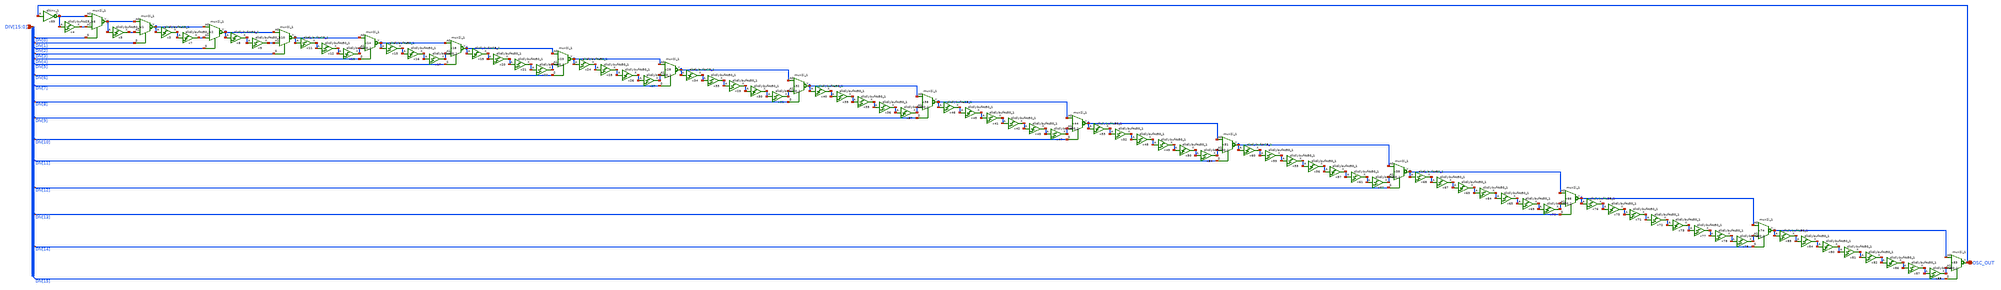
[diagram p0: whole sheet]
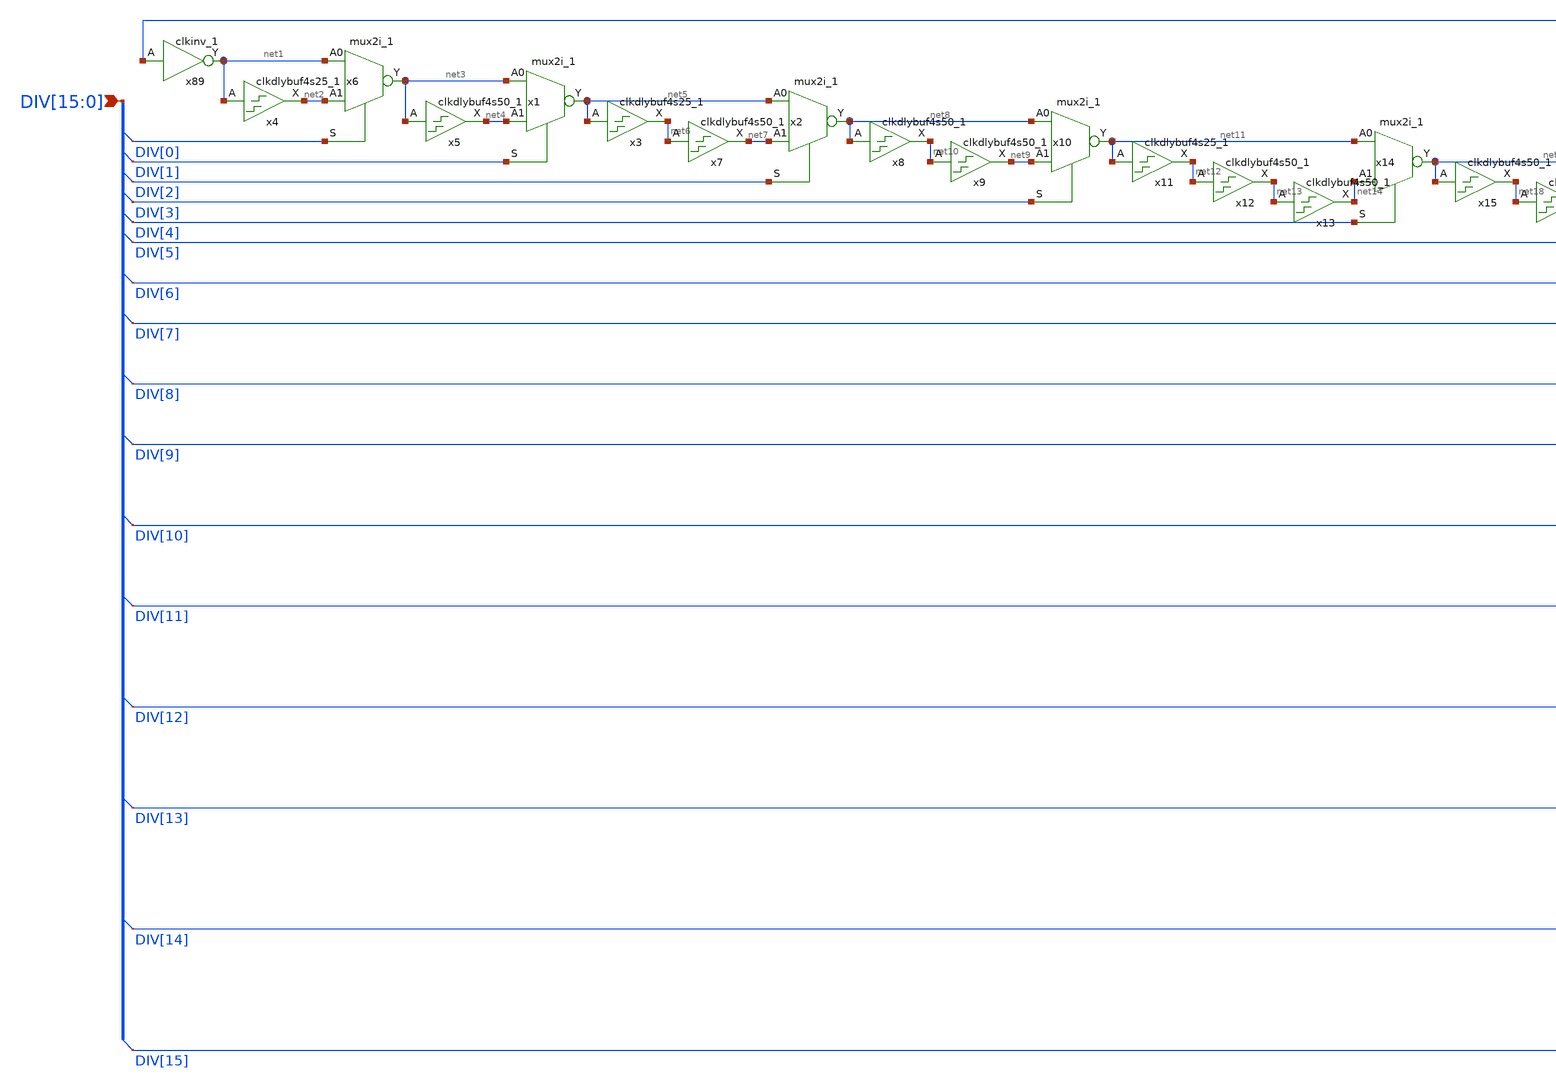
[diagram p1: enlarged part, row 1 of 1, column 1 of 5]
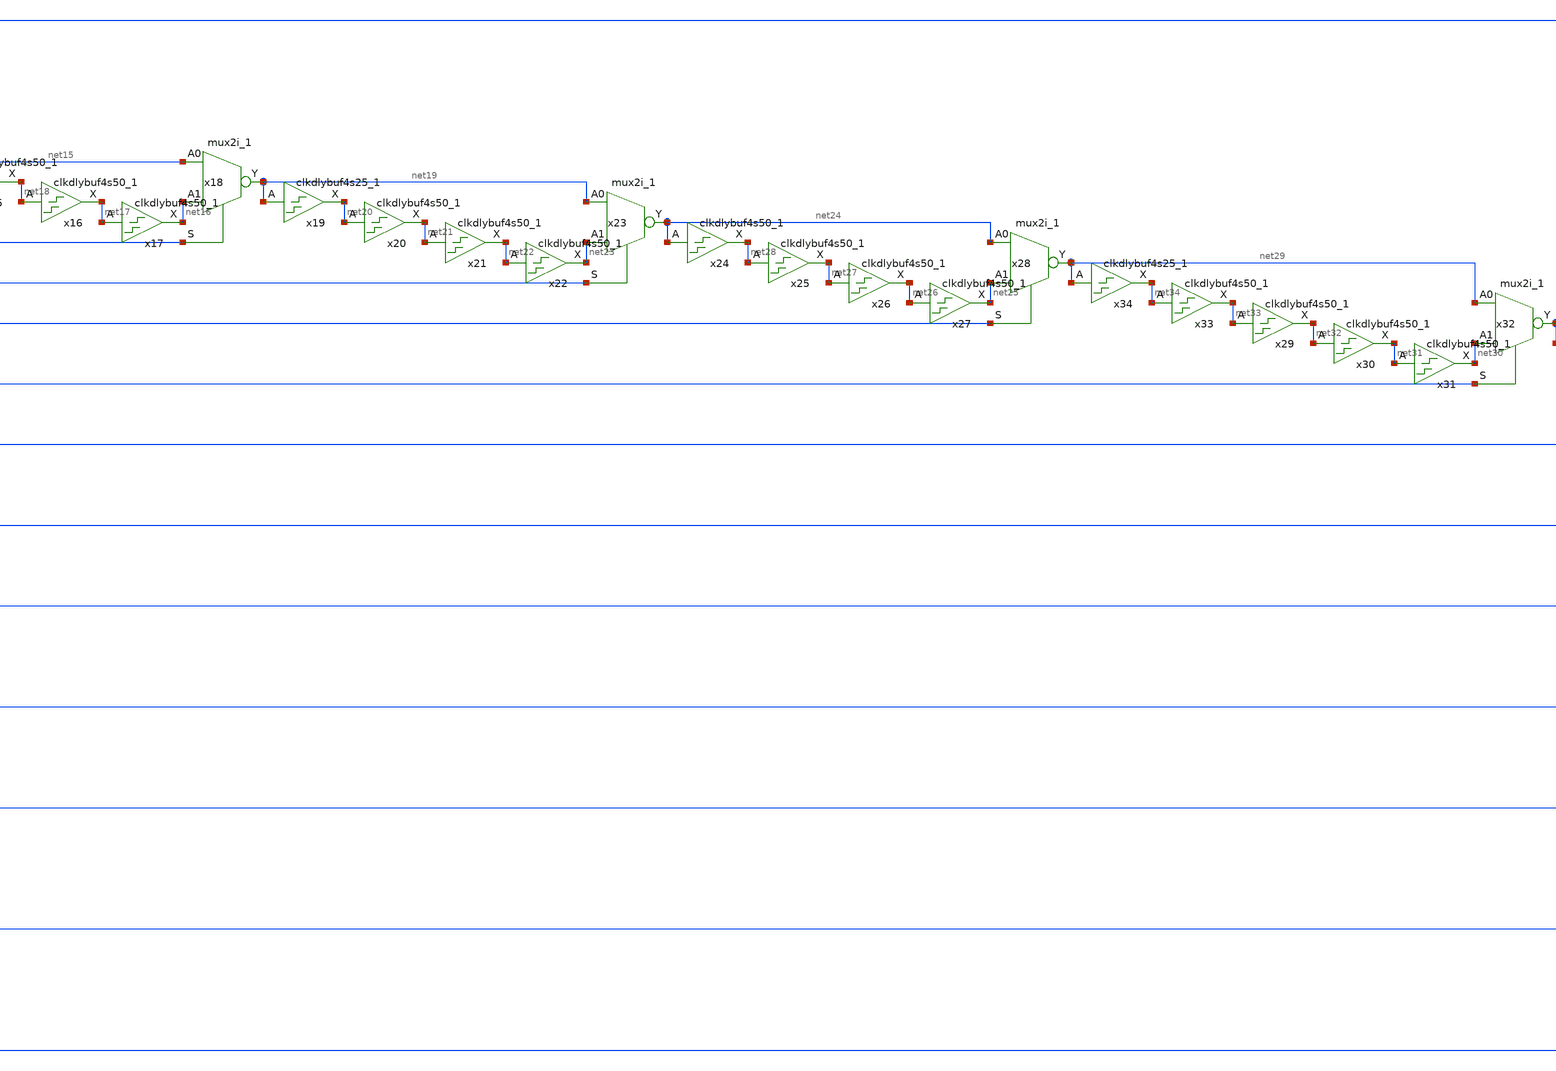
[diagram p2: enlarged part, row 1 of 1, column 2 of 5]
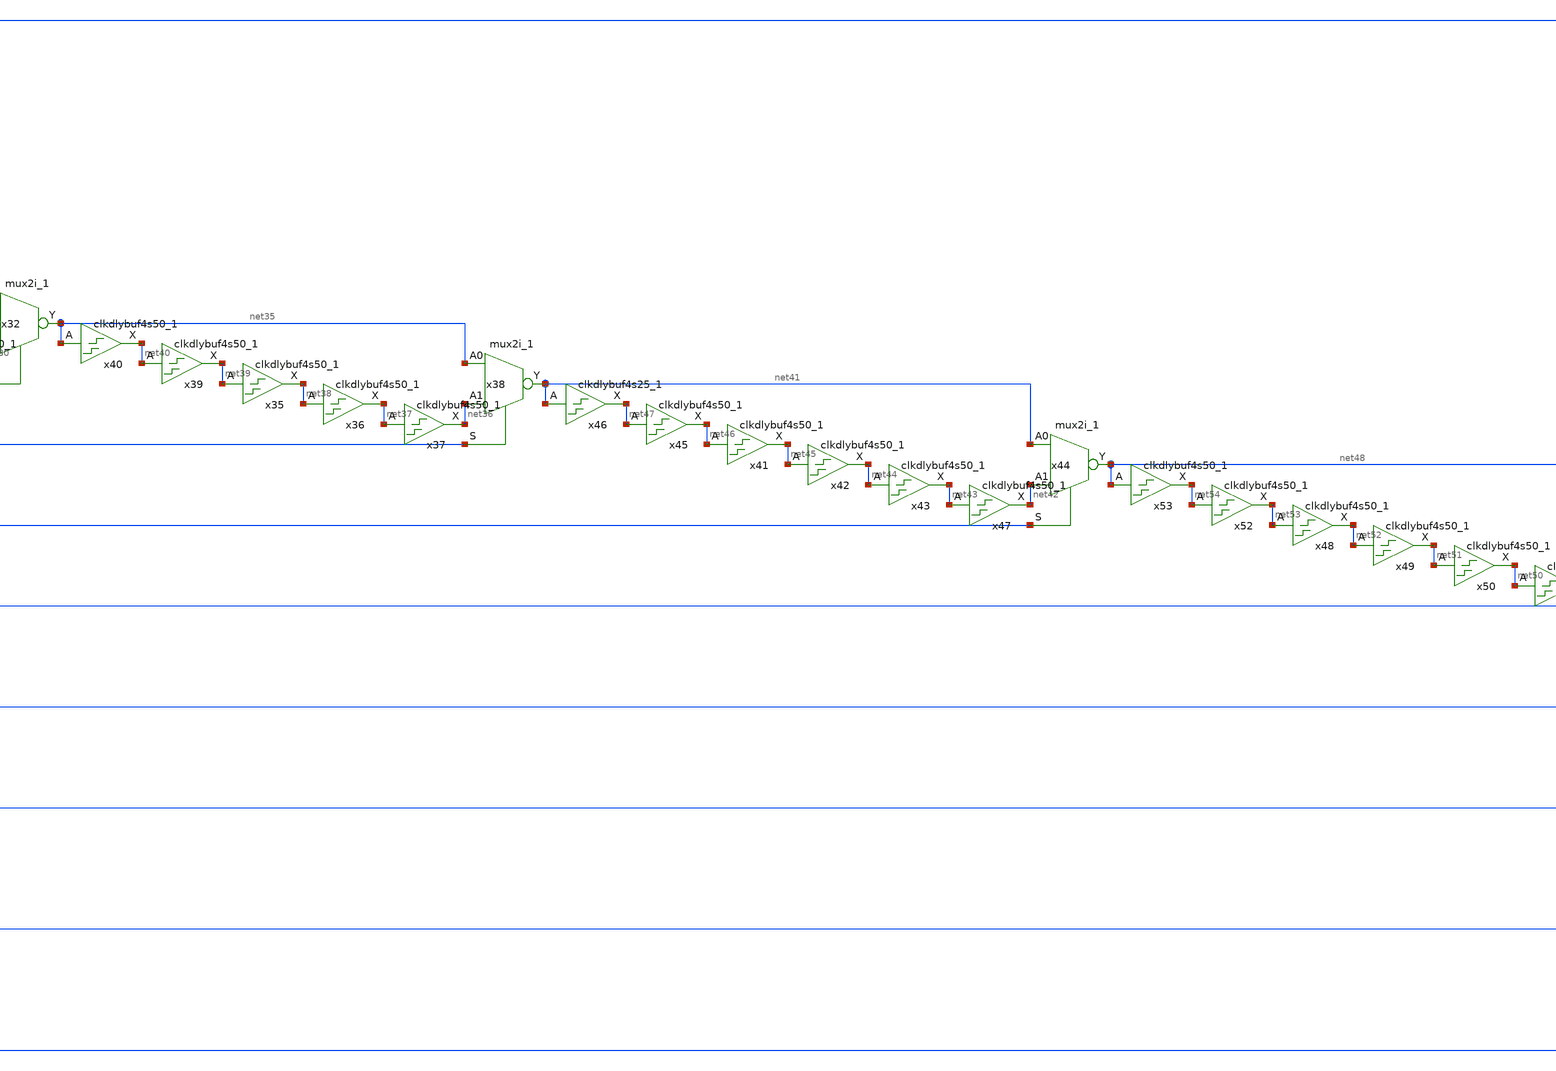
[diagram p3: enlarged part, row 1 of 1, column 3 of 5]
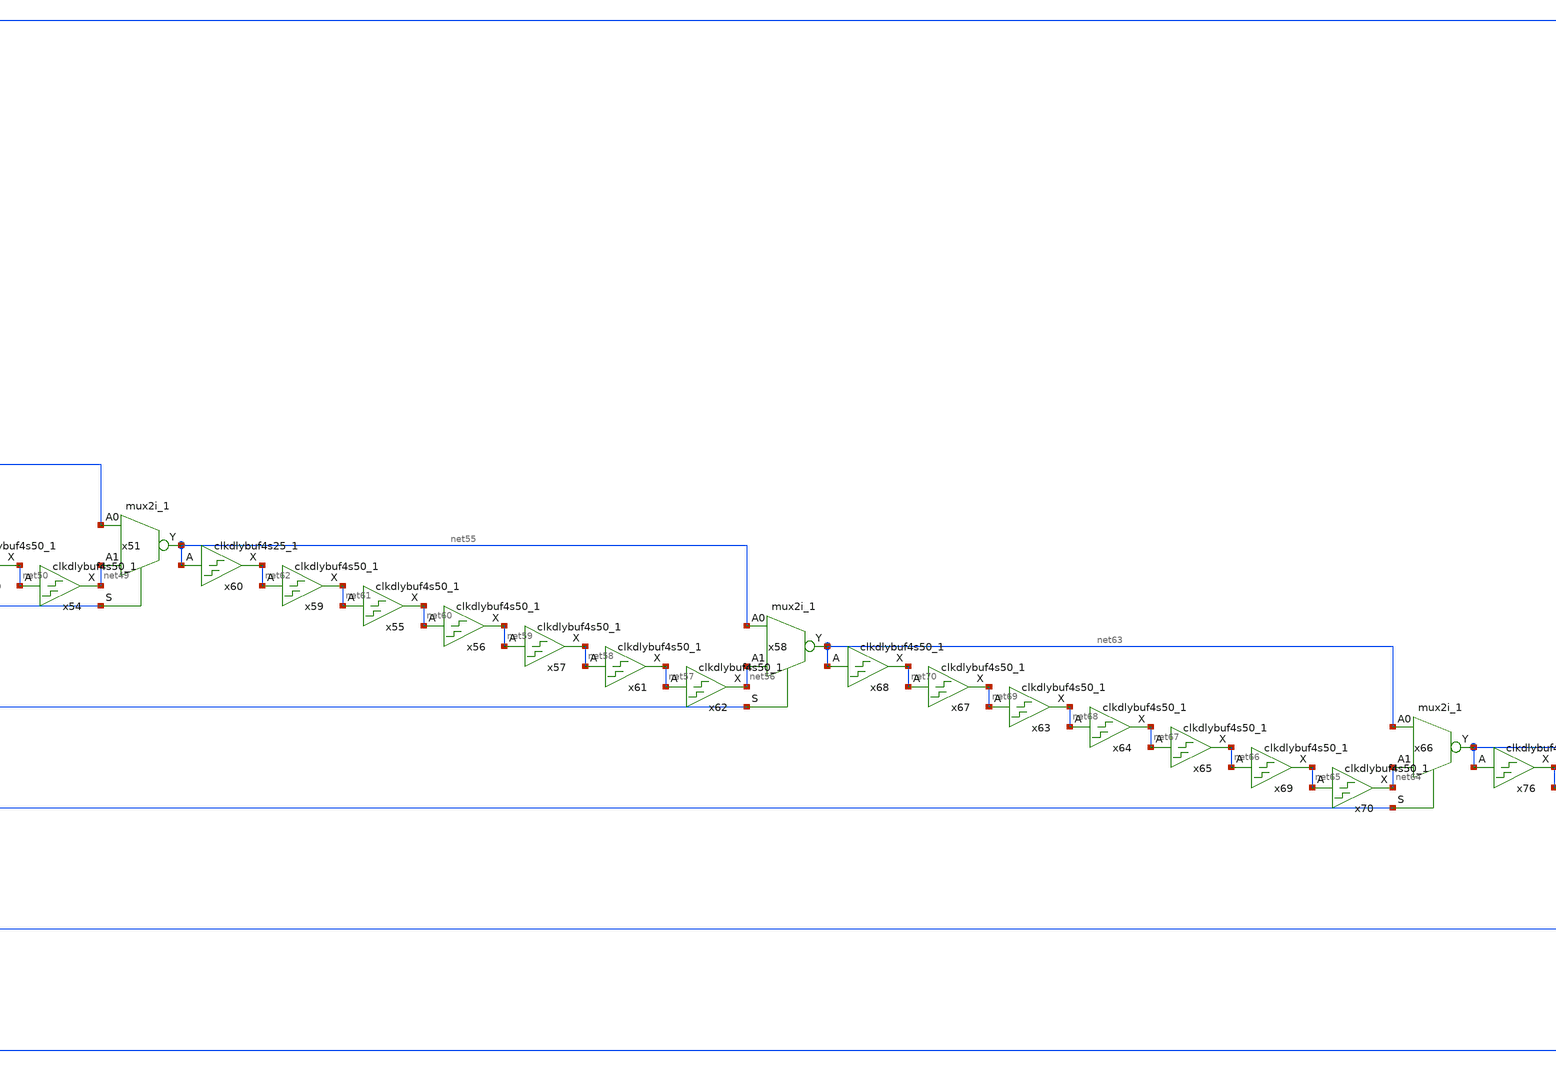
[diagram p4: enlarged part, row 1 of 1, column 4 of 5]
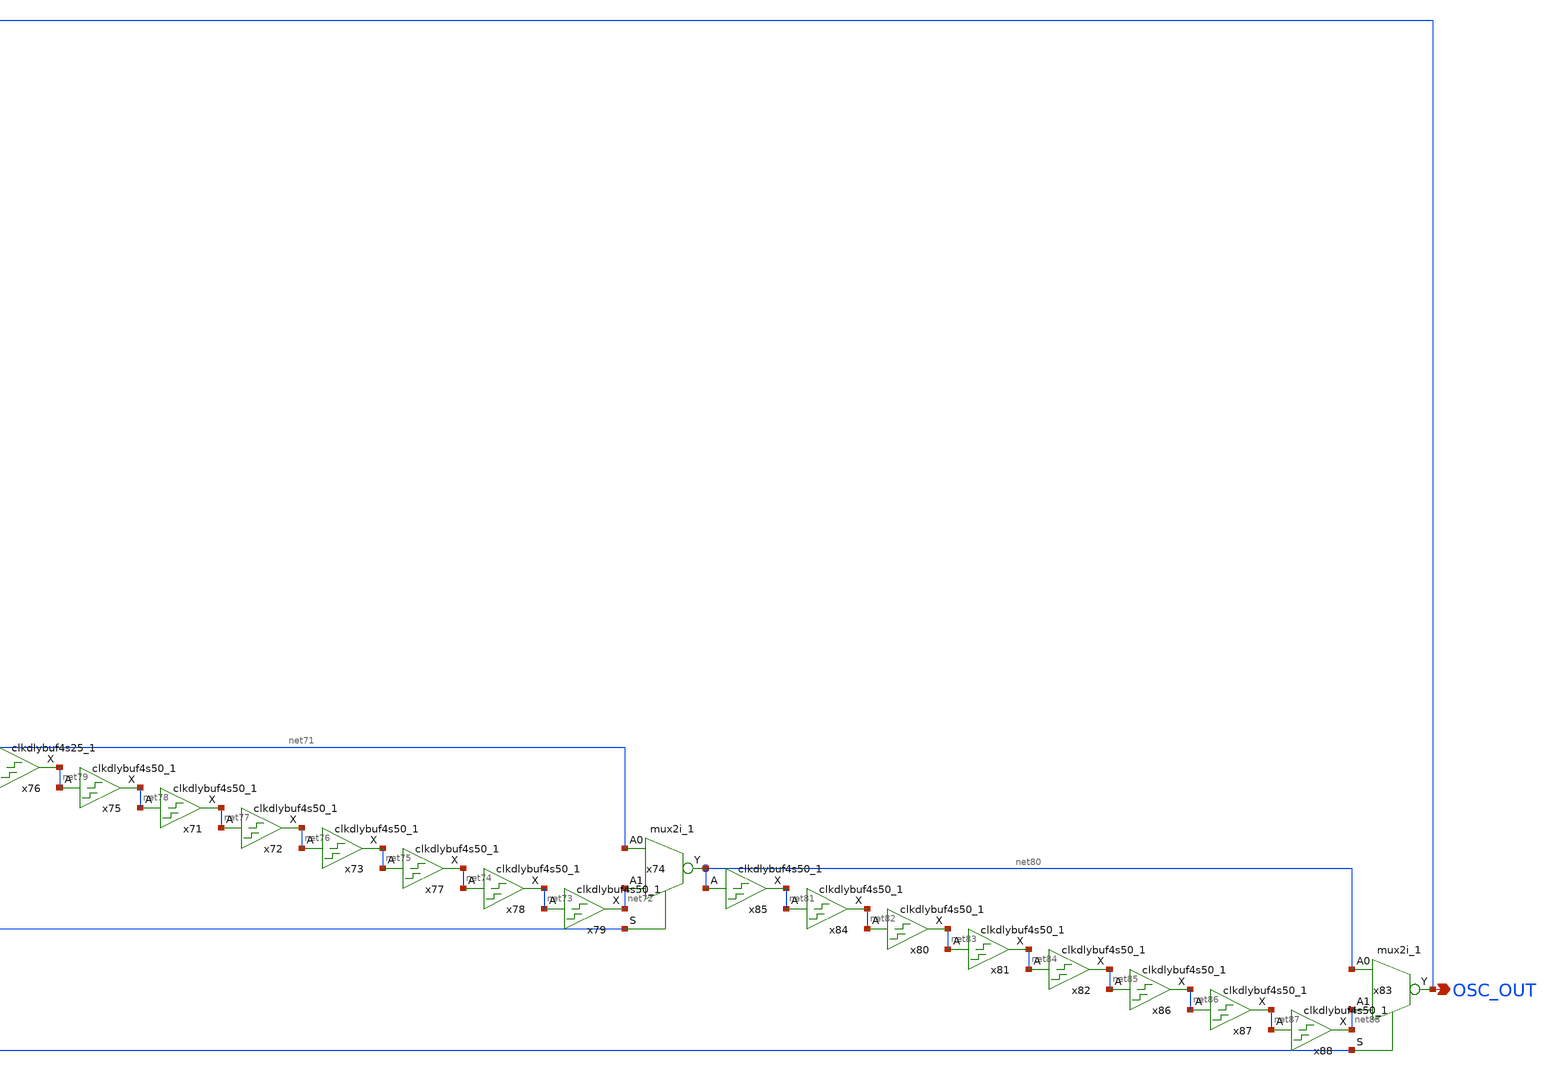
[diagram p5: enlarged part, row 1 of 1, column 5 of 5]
** sch_path: ring_osc.sch
**.subckt ring_osc OSC_OUT
*+ DIV[15],DIV[14],DIV[13],DIV[12],DIV[11],DIV[10],DIV[9],DIV[8],DIV[7],DIV[6],DIV[5],DIV[4],DIV[3],DIV[2],DIV[1],DIV[0]
*.opin OSC_OUT
*.ipin
*+ DIV[15],DIV[14],DIV[13],DIV[12],DIV[11],DIV[10],DIV[9],DIV[8],DIV[7],DIV[6],DIV[5],DIV[4],DIV[3],DIV[2],DIV[1],DIV[0]
x4 net1 VGND VNB VPB VPWR net2 sky130_fd_sc_hd__clkdlybuf4s25_1
x5 net3 VGND VNB VPB VPWR net4 sky130_fd_sc_hd__clkdlybuf4s50_1
x6 net1 net2 DIV[0] VGND VNB VPB VPWR net3 sky130_fd_sc_hd__mux2i_1
x1 net3 net4 DIV[1] VGND VNB VPB VPWR net5 sky130_fd_sc_hd__mux2i_1
x2 net5 net7 DIV[2] VGND VNB VPB VPWR net8 sky130_fd_sc_hd__mux2i_1
x3 net5 VGND VNB VPB VPWR net6 sky130_fd_sc_hd__clkdlybuf4s25_1
x7 net6 VGND VNB VPB VPWR net7 sky130_fd_sc_hd__clkdlybuf4s50_1
x8 net8 VGND VNB VPB VPWR net10 sky130_fd_sc_hd__clkdlybuf4s50_1
x9 net10 VGND VNB VPB VPWR net9 sky130_fd_sc_hd__clkdlybuf4s50_1
x10 net8 net9 DIV[3] VGND VNB VPB VPWR net11 sky130_fd_sc_hd__mux2i_1
x11 net11 VGND VNB VPB VPWR net12 sky130_fd_sc_hd__clkdlybuf4s25_1
x12 net12 VGND VNB VPB VPWR net13 sky130_fd_sc_hd__clkdlybuf4s50_1
x13 net13 VGND VNB VPB VPWR net14 sky130_fd_sc_hd__clkdlybuf4s50_1
x14 net11 net14 DIV[4] VGND VNB VPB VPWR net15 sky130_fd_sc_hd__mux2i_1
x15 net15 VGND VNB VPB VPWR net18 sky130_fd_sc_hd__clkdlybuf4s50_1
x16 net18 VGND VNB VPB VPWR net17 sky130_fd_sc_hd__clkdlybuf4s50_1
x17 net17 VGND VNB VPB VPWR net16 sky130_fd_sc_hd__clkdlybuf4s50_1
x18 net15 net16 DIV[5] VGND VNB VPB VPWR net19 sky130_fd_sc_hd__mux2i_1
x19 net19 VGND VNB VPB VPWR net20 sky130_fd_sc_hd__clkdlybuf4s25_1
x20 net20 VGND VNB VPB VPWR net21 sky130_fd_sc_hd__clkdlybuf4s50_1
x21 net21 VGND VNB VPB VPWR net22 sky130_fd_sc_hd__clkdlybuf4s50_1
x22 net22 VGND VNB VPB VPWR net23 sky130_fd_sc_hd__clkdlybuf4s50_1
x23 net19 net23 DIV[6] VGND VNB VPB VPWR net24 sky130_fd_sc_hd__mux2i_1
x25 net28 VGND VNB VPB VPWR net27 sky130_fd_sc_hd__clkdlybuf4s50_1
x26 net27 VGND VNB VPB VPWR net26 sky130_fd_sc_hd__clkdlybuf4s50_1
x27 net26 VGND VNB VPB VPWR net25 sky130_fd_sc_hd__clkdlybuf4s50_1
x28 net24 net25 DIV[7] VGND VNB VPB VPWR net29 sky130_fd_sc_hd__mux2i_1
x24 net24 VGND VNB VPB VPWR net28 sky130_fd_sc_hd__clkdlybuf4s50_1
x29 net33 VGND VNB VPB VPWR net32 sky130_fd_sc_hd__clkdlybuf4s50_1
x30 net32 VGND VNB VPB VPWR net31 sky130_fd_sc_hd__clkdlybuf4s50_1
x31 net31 VGND VNB VPB VPWR net30 sky130_fd_sc_hd__clkdlybuf4s50_1
x32 net29 net30 DIV[8] VGND VNB VPB VPWR net35 sky130_fd_sc_hd__mux2i_1
x33 net34 VGND VNB VPB VPWR net33 sky130_fd_sc_hd__clkdlybuf4s50_1
x34 net29 VGND VNB VPB VPWR net34 sky130_fd_sc_hd__clkdlybuf4s25_1
x35 net39 VGND VNB VPB VPWR net38 sky130_fd_sc_hd__clkdlybuf4s50_1
x36 net38 VGND VNB VPB VPWR net37 sky130_fd_sc_hd__clkdlybuf4s50_1
x37 net37 VGND VNB VPB VPWR net36 sky130_fd_sc_hd__clkdlybuf4s50_1
x38 net35 net36 DIV[9] VGND VNB VPB VPWR net41 sky130_fd_sc_hd__mux2i_1
x39 net40 VGND VNB VPB VPWR net39 sky130_fd_sc_hd__clkdlybuf4s50_1
x41 net46 VGND VNB VPB VPWR net45 sky130_fd_sc_hd__clkdlybuf4s50_1
x42 net45 VGND VNB VPB VPWR net44 sky130_fd_sc_hd__clkdlybuf4s50_1
x43 net44 VGND VNB VPB VPWR net43 sky130_fd_sc_hd__clkdlybuf4s50_1
x44 net41 net42 DIV[10] VGND VNB VPB VPWR net48 sky130_fd_sc_hd__mux2i_1
x45 net47 VGND VNB VPB VPWR net46 sky130_fd_sc_hd__clkdlybuf4s50_1
x46 net41 VGND VNB VPB VPWR net47 sky130_fd_sc_hd__clkdlybuf4s25_1
x47 net43 VGND VNB VPB VPWR net42 sky130_fd_sc_hd__clkdlybuf4s50_1
x48 net53 VGND VNB VPB VPWR net52 sky130_fd_sc_hd__clkdlybuf4s50_1
x49 net52 VGND VNB VPB VPWR net51 sky130_fd_sc_hd__clkdlybuf4s50_1
x50 net51 VGND VNB VPB VPWR net50 sky130_fd_sc_hd__clkdlybuf4s50_1
x51 net48 net49 DIV[11] VGND VNB VPB VPWR net55 sky130_fd_sc_hd__mux2i_1
x52 net54 VGND VNB VPB VPWR net53 sky130_fd_sc_hd__clkdlybuf4s50_1
x54 net50 VGND VNB VPB VPWR net49 sky130_fd_sc_hd__clkdlybuf4s50_1
x55 net61 VGND VNB VPB VPWR net60 sky130_fd_sc_hd__clkdlybuf4s50_1
x56 net60 VGND VNB VPB VPWR net59 sky130_fd_sc_hd__clkdlybuf4s50_1
x57 net59 VGND VNB VPB VPWR net58 sky130_fd_sc_hd__clkdlybuf4s50_1
x58 net55 net56 DIV[12] VGND VNB VPB VPWR net63 sky130_fd_sc_hd__mux2i_1
x59 net62 VGND VNB VPB VPWR net61 sky130_fd_sc_hd__clkdlybuf4s50_1
x60 net55 VGND VNB VPB VPWR net62 sky130_fd_sc_hd__clkdlybuf4s25_1
x61 net58 VGND VNB VPB VPWR net57 sky130_fd_sc_hd__clkdlybuf4s50_1
x62 net57 VGND VNB VPB VPWR net56 sky130_fd_sc_hd__clkdlybuf4s50_1
x63 net69 VGND VNB VPB VPWR net68 sky130_fd_sc_hd__clkdlybuf4s50_1
x64 net68 VGND VNB VPB VPWR net67 sky130_fd_sc_hd__clkdlybuf4s50_1
x65 net67 VGND VNB VPB VPWR net66 sky130_fd_sc_hd__clkdlybuf4s50_1
x66 net63 net64 DIV[13] VGND VNB VPB VPWR net71 sky130_fd_sc_hd__mux2i_1
x67 net70 VGND VNB VPB VPWR net69 sky130_fd_sc_hd__clkdlybuf4s50_1
x69 net66 VGND VNB VPB VPWR net65 sky130_fd_sc_hd__clkdlybuf4s50_1
x70 net65 VGND VNB VPB VPWR net64 sky130_fd_sc_hd__clkdlybuf4s50_1
x71 net78 VGND VNB VPB VPWR net77 sky130_fd_sc_hd__clkdlybuf4s50_1
x72 net77 VGND VNB VPB VPWR net76 sky130_fd_sc_hd__clkdlybuf4s50_1
x73 net76 VGND VNB VPB VPWR net75 sky130_fd_sc_hd__clkdlybuf4s50_1
x74 net71 net72 DIV[14] VGND VNB VPB VPWR net80 sky130_fd_sc_hd__mux2i_1
x75 net79 VGND VNB VPB VPWR net78 sky130_fd_sc_hd__clkdlybuf4s50_1
x76 net71 VGND VNB VPB VPWR net79 sky130_fd_sc_hd__clkdlybuf4s25_1
x77 net75 VGND VNB VPB VPWR net74 sky130_fd_sc_hd__clkdlybuf4s50_1
x78 net74 VGND VNB VPB VPWR net73 sky130_fd_sc_hd__clkdlybuf4s50_1
x79 net73 VGND VNB VPB VPWR net72 sky130_fd_sc_hd__clkdlybuf4s50_1
x80 net82 VGND VNB VPB VPWR net83 sky130_fd_sc_hd__clkdlybuf4s50_1
x81 net83 VGND VNB VPB VPWR net84 sky130_fd_sc_hd__clkdlybuf4s50_1
x82 net84 VGND VNB VPB VPWR net85 sky130_fd_sc_hd__clkdlybuf4s50_1
x83 net80 net88 DIV[15] VGND VNB VPB VPWR OSC_OUT sky130_fd_sc_hd__mux2i_1
x84 net81 VGND VNB VPB VPWR net82 sky130_fd_sc_hd__clkdlybuf4s50_1
x86 net85 VGND VNB VPB VPWR net86 sky130_fd_sc_hd__clkdlybuf4s50_1
x87 net86 VGND VNB VPB VPWR net87 sky130_fd_sc_hd__clkdlybuf4s50_1
x88 net87 VGND VNB VPB VPWR net88 sky130_fd_sc_hd__clkdlybuf4s50_1
x89 OSC_OUT VGND VNB VPB VPWR net1 sky130_fd_sc_hd__clkinv_1
x40 net35 VGND VNB VPB VPWR net40 sky130_fd_sc_hd__clkdlybuf4s50_1
x53 net48 VGND VNB VPB VPWR net54 sky130_fd_sc_hd__clkdlybuf4s50_1
x68 net63 VGND VNB VPB VPWR net70 sky130_fd_sc_hd__clkdlybuf4s50_1
x85 net80 VGND VNB VPB VPWR net81 sky130_fd_sc_hd__clkdlybuf4s50_1
**.ends
.end
